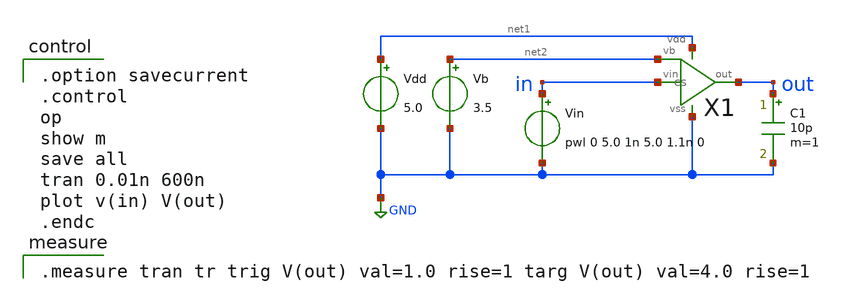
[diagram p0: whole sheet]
** sch_path: OR1/PTC06/opamp/cs_tran.sch
**.subckt cs_tran
Vdd net1 GND 5.0
Vb net2 GND 3.5
X1 in net2 out net1 GND cs
C1 out GND 10p m=1
Vin in GND pwl 0 5.0 1n 5.0 1.1n 0
**** begin user architecture code

.option savecurrent
.control
op
show m
save all
tran 0.01n 600n
plot v(in) V(out)
.endc


.measure tran tr trig V(out) val=1.0 rise=1 targ V(out) val=4.0 rise=1

 .include $::LIB/mos.lib
.include $::LIB/passive.lib
.include $::LIB/diode.lib
**** end user architecture code
**.ends

* expanding   symbol:  cs.sym # of pins=5
** sym_path: cs.sym
** sch_path: cs.sch
.subckt cs vin vb out vdd vss
*.ipin vb
*.ipin vin
*.opin out
*.iopin vss
*.iopin vdd
M6 out vb vdd vdd pmos L=2u W=400u m=1
M7 out vin vss vss nmos L=2u W=200u m=1
.ends

.GLOBAL GND
.end
